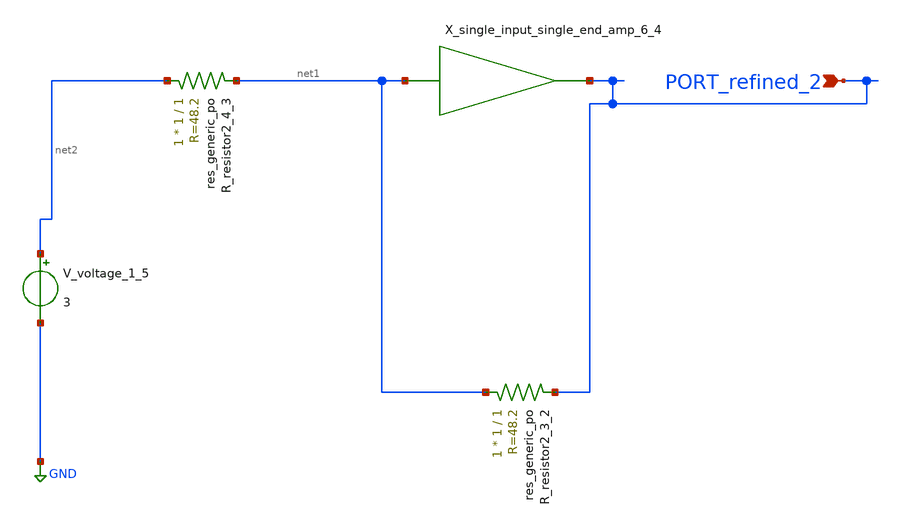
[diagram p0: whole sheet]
** sch_path: schematics/AMSNet/605.sch
**.subckt 605 PORT_refined_2
*.ipin PORT_refined_2
XR_resistor2_3_2 net1 PORT_refined_2 sky130_fd_pr__res_generic_po W=1 L=1 m=1
XR_resistor2_4_3 net2 net1 sky130_fd_pr__res_generic_po W=1 L=1 m=1
X_single_input_single_end_amp_6_4 net1 PORT_refined_2 schemgen_siso_amp
V_voltage_1_5 net2 GND 3
**.ends

* expanding   symbol:  schemgen_siso_amp.sym # of pins=2
** sym_path: symbols/schemgen_siso_amp.sym
.subckt schemgen_siso_amp IN OUT
* SchemGen ideal single-input amplifier: Vout = 1e5 * V(IN)
E1 OUT 0 IN 0 1e5
.ends schemgen_siso_amp
.GLOBAL GND
.end
